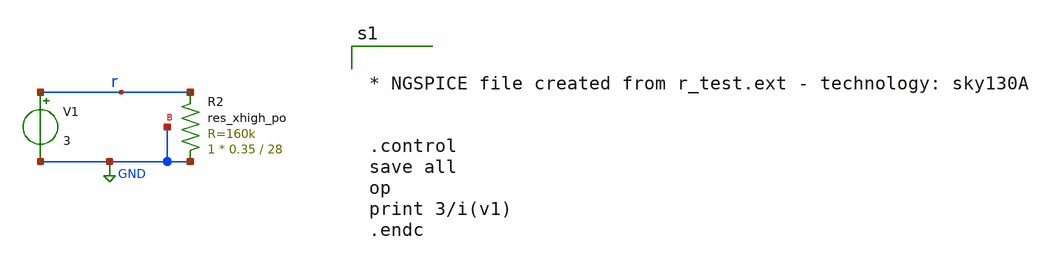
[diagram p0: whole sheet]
** sch_path: xschem/src/rctest.sch
**.subckt rctest
V1 r GND 3
XR2 GND r GND sky130_fd_pr__res_xhigh_po W=0.35 L=28 mult=1 m=1
**** begin user architecture code

.include /home/eda/pdk/skywater-pdk/libraries/sky130_fd_pr_ngspice/latest/models/corners/tt.spice
.include /home/eda/magic/test/r_test.spice
* Resistor$::SKYWATER_MODELS/Capacitor
.include $::SKYWATER_MODELS/models/r+c/res_typical__cap_typical.spice
.include $::SKYWATER_MODELS/models/r+c/res_typical__cap_typical__lin.spice
* Special cells
.include $::SKYWATER_MODELS/models/corners/tt/specialized_cells.spice





* NGSPICE file created from r_test.ext - technology: sky130A


.control
save all
op
print 3/i(v1)
.endc



**** end user architecture code
**.ends
.GLOBAL GND
.end
